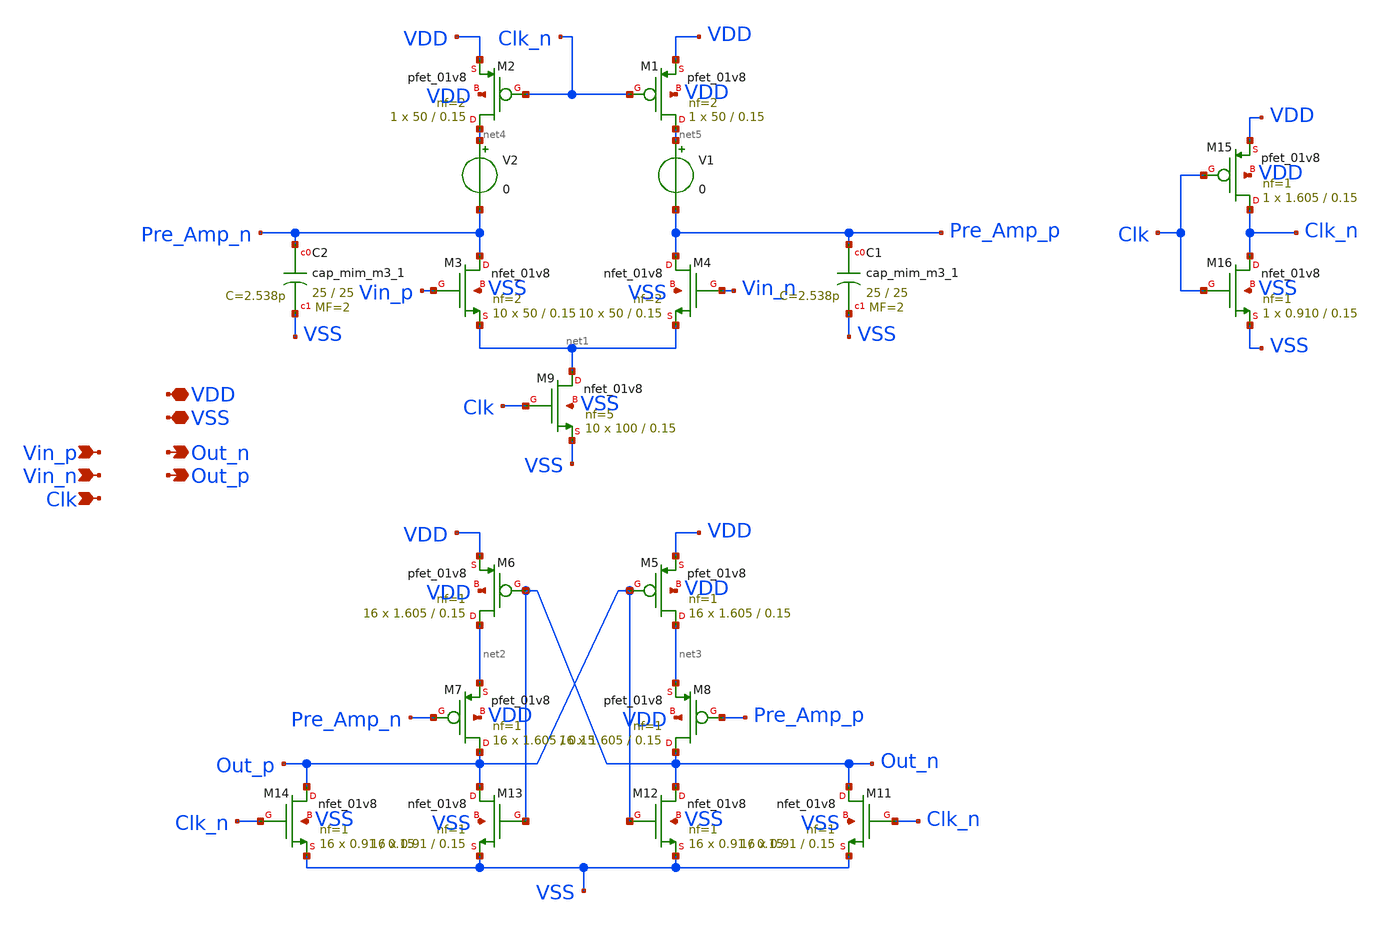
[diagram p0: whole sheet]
** sch_path: xschem/src/comparator/comparator.sch
**.subckt comparator VDD VSS Vin_p Out_n Vin_n Out_p Clk
*.iopin VDD
*.iopin VSS
*.ipin Vin_p
*.opin Out_n
*.ipin Vin_n
*.opin Out_p
*.ipin Clk
XM1 net5 Clk_n VDD VDD sky130_fd_pr__pfet_01v8 L=0.15 W=50 nf=2 ad='int((nf+1)/2) * W/nf * 0.29' as='int((nf+2)/2) * W/nf * 0.29'
+ pd='2*int((nf+1)/2) * (W/nf + 0.29)' ps='2*int((nf+2)/2) * (W/nf + 0.29)' nrd='0.29 / W' nrs='0.29 / W'
+ sa=0 sb=0 sd=0 mult=1 m=1
XM2 net4 Clk_n VDD VDD sky130_fd_pr__pfet_01v8 L=0.15 W=50 nf=2 ad='int((nf+1)/2) * W/nf * 0.29' as='int((nf+2)/2) * W/nf * 0.29'
+ pd='2*int((nf+1)/2) * (W/nf + 0.29)' ps='2*int((nf+2)/2) * (W/nf + 0.29)' nrd='0.29 / W' nrs='0.29 / W'
+ sa=0 sb=0 sd=0 mult=1 m=1
XM3 Pre_Amp_n Vin_p net1 VSS sky130_fd_pr__nfet_01v8 L=0.15 W=50 nf=2 ad='int((nf+1)/2) * W/nf * 0.29'
+ as='int((nf+2)/2) * W/nf * 0.29' pd='2*int((nf+1)/2) * (W/nf + 0.29)' ps='2*int((nf+2)/2) * (W/nf + 0.29)'
+ nrd='0.29 / W' nrs='0.29 / W' sa=0 sb=0 sd=0 mult=10 m=10
XM4 Pre_Amp_p Vin_n net1 VSS sky130_fd_pr__nfet_01v8 L=0.15 W=50 nf=2 ad='int((nf+1)/2) * W/nf * 0.29'
+ as='int((nf+2)/2) * W/nf * 0.29' pd='2*int((nf+1)/2) * (W/nf + 0.29)' ps='2*int((nf+2)/2) * (W/nf + 0.29)'
+ nrd='0.29 / W' nrs='0.29 / W' sa=0 sb=0 sd=0 mult=10 m=10
XM5 net3 Out_p VDD VDD sky130_fd_pr__pfet_01v8 L=0.15 W=1.605 nf=1 ad='int((nf+1)/2) * W/nf * 0.29' as='int((nf+2)/2) * W/nf * 0.29'
+ pd='2*int((nf+1)/2) * (W/nf + 0.29)' ps='2*int((nf+2)/2) * (W/nf + 0.29)' nrd='0.29 / W' nrs='0.29 / W'
+ sa=0 sb=0 sd=0 mult=16 m=16
XM6 net2 Out_n VDD VDD sky130_fd_pr__pfet_01v8 L=0.15 W=1.605 nf=1 ad='int((nf+1)/2) * W/nf * 0.29' as='int((nf+2)/2) * W/nf * 0.29'
+ pd='2*int((nf+1)/2) * (W/nf + 0.29)' ps='2*int((nf+2)/2) * (W/nf + 0.29)' nrd='0.29 / W' nrs='0.29 / W'
+ sa=0 sb=0 sd=0 mult=16 m=16
XM9 net1 Clk VSS VSS sky130_fd_pr__nfet_01v8 L=0.15 W=100 nf=5 ad='int((nf+1)/2) * W/nf * 0.29' as='int((nf+2)/2) * W/nf * 0.29'
+ pd='2*int((nf+1)/2) * (W/nf + 0.29)' ps='2*int((nf+2)/2) * (W/nf + 0.29)' nrd='0.29 / W' nrs='0.29 / W'
+ sa=0 sb=0 sd=0 mult=10 m=10
XM11 Out_n Clk_n VSS VSS sky130_fd_pr__nfet_01v8 L=0.15 W=0.91 nf=1 ad='int((nf+1)/2) * W/nf * 0.29'
+ as='int((nf+2)/2) * W/nf * 0.29' pd='2*int((nf+1)/2) * (W/nf + 0.29)' ps='2*int((nf+2)/2) * (W/nf + 0.29)'
+ nrd='0.29 / W' nrs='0.29 / W' sa=0 sb=0 sd=0 mult=16 m=16
XM12 Out_n Out_p VSS VSS sky130_fd_pr__nfet_01v8 L=0.15 W=0.91 nf=1 ad='int((nf+1)/2) * W/nf * 0.29'
+ as='int((nf+2)/2) * W/nf * 0.29' pd='2*int((nf+1)/2) * (W/nf + 0.29)' ps='2*int((nf+2)/2) * (W/nf + 0.29)'
+ nrd='0.29 / W' nrs='0.29 / W' sa=0 sb=0 sd=0 mult=16 m=16
XM13 Out_p Out_n VSS VSS sky130_fd_pr__nfet_01v8 L=0.15 W=0.91 nf=1 ad='int((nf+1)/2) * W/nf * 0.29'
+ as='int((nf+2)/2) * W/nf * 0.29' pd='2*int((nf+1)/2) * (W/nf + 0.29)' ps='2*int((nf+2)/2) * (W/nf + 0.29)'
+ nrd='0.29 / W' nrs='0.29 / W' sa=0 sb=0 sd=0 mult=16 m=16
XM14 Out_p Clk_n VSS VSS sky130_fd_pr__nfet_01v8 L=0.15 W=0.91 nf=1 ad='int((nf+1)/2) * W/nf * 0.29'
+ as='int((nf+2)/2) * W/nf * 0.29' pd='2*int((nf+1)/2) * (W/nf + 0.29)' ps='2*int((nf+2)/2) * (W/nf + 0.29)'
+ nrd='0.29 / W' nrs='0.29 / W' sa=0 sb=0 sd=0 mult=16 m=16
XM15 Clk_n Clk VDD VDD sky130_fd_pr__pfet_01v8 L=0.15 W=1.605 nf=1 ad='int((nf+1)/2) * W/nf * 0.29' as='int((nf+2)/2) * W/nf * 0.29'
+ pd='2*int((nf+1)/2) * (W/nf + 0.29)' ps='2*int((nf+2)/2) * (W/nf + 0.29)' nrd='0.29 / W' nrs='0.29 / W'
+ sa=0 sb=0 sd=0 mult=1 m=1
XM16 Clk_n Clk VSS VSS sky130_fd_pr__nfet_01v8 L=0.15 W=0.910 nf=1 ad='int((nf+1)/2) * W/nf * 0.29' as='int((nf+2)/2) * W/nf * 0.29'
+ pd='2*int((nf+1)/2) * (W/nf + 0.29)' ps='2*int((nf+2)/2) * (W/nf + 0.29)' nrd='0.29 / W' nrs='0.29 / W'
+ sa=0 sb=0 sd=0 mult=1 m=1
XM7 Out_p Pre_Amp_n net2 VDD sky130_fd_pr__pfet_01v8 L=0.15 W=1.605 nf=1 ad='int((nf+1)/2) * W/nf * 0.29'
+ as='int((nf+2)/2) * W/nf * 0.29' pd='2*int((nf+1)/2) * (W/nf + 0.29)' ps='2*int((nf+2)/2) * (W/nf + 0.29)'
+ nrd='0.29 / W' nrs='0.29 / W' sa=0 sb=0 sd=0 mult=16 m=16
XM8 Out_n Pre_Amp_p net3 VDD sky130_fd_pr__pfet_01v8 L=0.15 W=1.605 nf=1 ad='int((nf+1)/2) * W/nf * 0.29'
+ as='int((nf+2)/2) * W/nf * 0.29' pd='2*int((nf+1)/2) * (W/nf + 0.29)' ps='2*int((nf+2)/2) * (W/nf + 0.29)'
+ nrd='0.29 / W' nrs='0.29 / W' sa=0 sb=0 sd=0 mult=16 m=16
V1 net5 Pre_Amp_p 0
V2 net4 Pre_Amp_n 0
XC1 Pre_Amp_p VSS sky130_fd_pr__cap_mim_m3_1 W=25 L=25 MF=2 m=2
XC2 Pre_Amp_n VSS sky130_fd_pr__cap_mim_m3_1 W=25 L=25 MF=2 m=2
**.ends
.end
